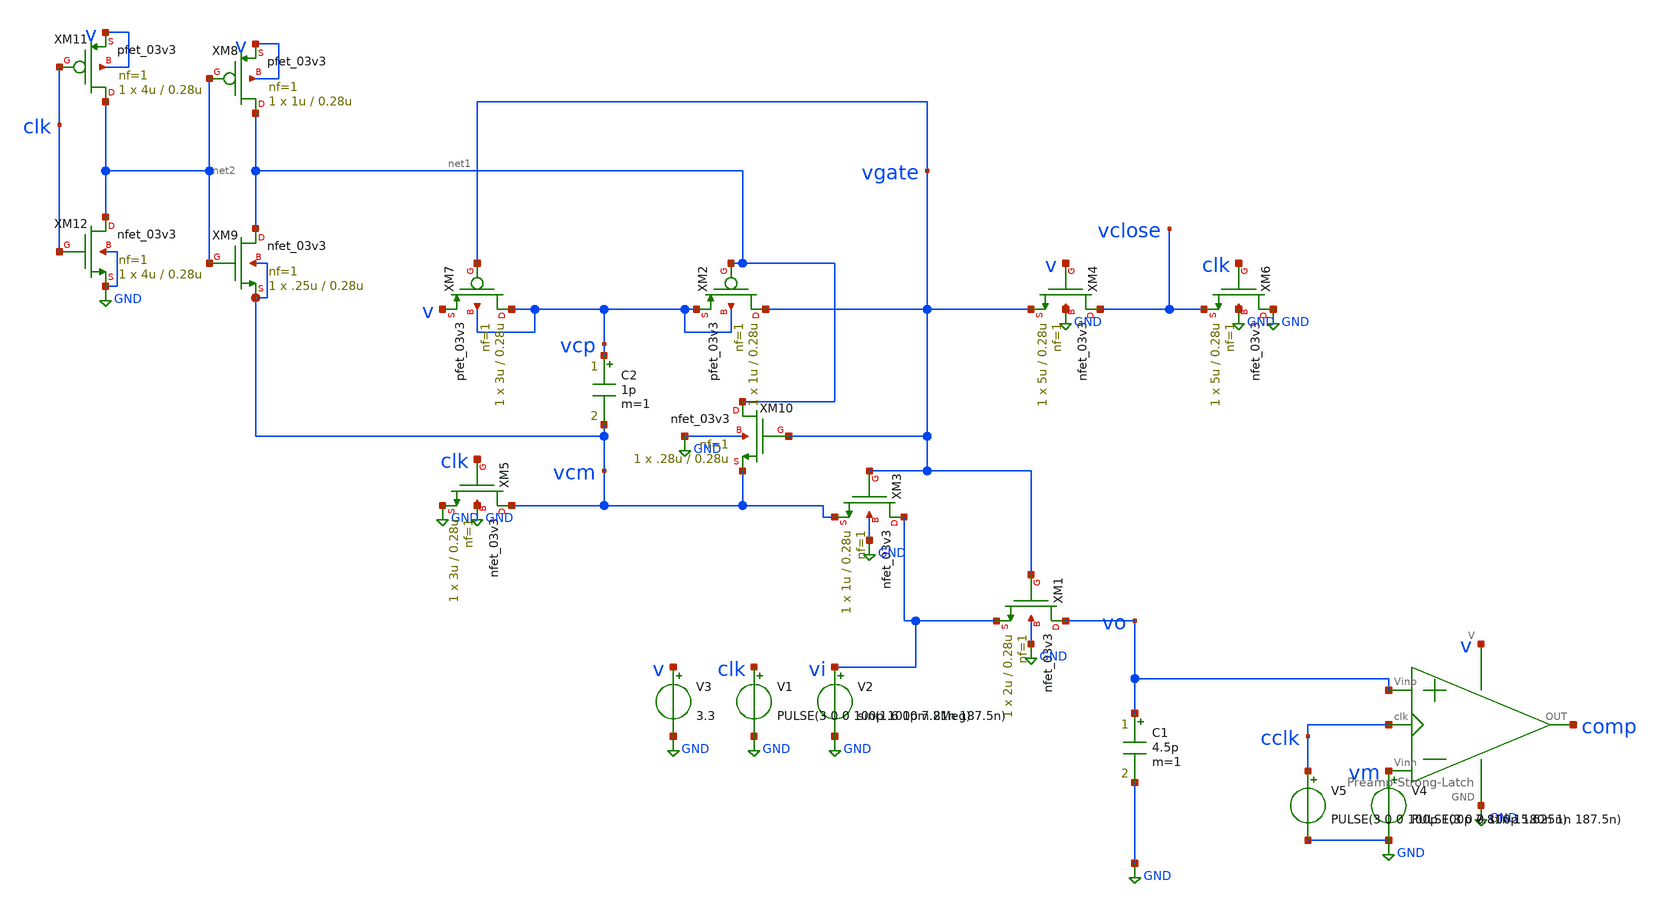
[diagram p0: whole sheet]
** sch_path: full_S&H/testbench/full__tb.sch
**.subckt full__tb
XM1 vo vgate vi GND nfet_03v3 L=0.28u W=2u nf=1 ad='int((nf+1)/2) * W/nf * 0.18u' as='int((nf+2)/2) * W/nf * 0.18u'
+ pd='2*int((nf+1)/2) * (W/nf + 0.18u)' ps='2*int((nf+2)/2) * (W/nf + 0.18u)' nrd='0.18u / W' nrs='0.18u / W'
+ sa=0 sb=0 sd=0 m=1
XM2 vgate net1 vcp vcp pfet_03v3 L=0.28u W=1u nf=1 ad='int((nf+1)/2) * W/nf * 0.18u' as='int((nf+2)/2) * W/nf * 0.18u'
+ pd='2*int((nf+1)/2) * (W/nf + 0.18u)' ps='2*int((nf+2)/2) * (W/nf + 0.18u)' nrd='0.18u / W' nrs='0.18u / W'
+ sa=0 sb=0 sd=0 m=1
XM3 vi vgate vcm GND nfet_03v3 L=0.28u W=1u nf=1 ad='int((nf+1)/2) * W/nf * 0.18u' as='int((nf+2)/2) * W/nf * 0.18u'
+ pd='2*int((nf+1)/2) * (W/nf + 0.18u)' ps='2*int((nf+2)/2) * (W/nf + 0.18u)' nrd='0.18u / W' nrs='0.18u / W'
+ sa=0 sb=0 sd=0 m=1
XM4 vclose v vgate GND nfet_03v3 L=0.28u W=5u nf=1 ad='int((nf+1)/2) * W/nf * 0.18u' as='int((nf+2)/2) * W/nf * 0.18u'
+ pd='2*int((nf+1)/2) * (W/nf + 0.18u)' ps='2*int((nf+2)/2) * (W/nf + 0.18u)' nrd='0.18u / W' nrs='0.18u / W'
+ sa=0 sb=0 sd=0 m=1
XM5 vcm clk GND GND nfet_03v3 L=0.28u W=3u nf=1 ad='int((nf+1)/2) * W/nf * 0.18u' as='int((nf+2)/2) * W/nf * 0.18u'
+ pd='2*int((nf+1)/2) * (W/nf + 0.18u)' ps='2*int((nf+2)/2) * (W/nf + 0.18u)' nrd='0.18u / W' nrs='0.18u / W'
+ sa=0 sb=0 sd=0 m=1
XM6 GND clk vclose GND nfet_03v3 L=0.28u W=5u nf=1 ad='int((nf+1)/2) * W/nf * 0.18u' as='int((nf+2)/2) * W/nf * 0.18u'
+ pd='2*int((nf+1)/2) * (W/nf + 0.18u)' ps='2*int((nf+2)/2) * (W/nf + 0.18u)' nrd='0.18u / W' nrs='0.18u / W'
+ sa=0 sb=0 sd=0 m=1
XM7 vcp vgate v vcp pfet_03v3 L=0.28u W=3u nf=1 ad='int((nf+1)/2) * W/nf * 0.18u' as='int((nf+2)/2) * W/nf * 0.18u'
+ pd='2*int((nf+1)/2) * (W/nf + 0.18u)' ps='2*int((nf+2)/2) * (W/nf + 0.18u)' nrd='0.18u / W' nrs='0.18u / W'
+ sa=0 sb=0 sd=0 m=1
XM8 net1 net2 v v pfet_03v3 L=0.28u W=1u nf=1 ad='int((nf+1)/2) * W/nf * 0.18u' as='int((nf+2)/2) * W/nf * 0.18u'
+ pd='2*int((nf+1)/2) * (W/nf + 0.18u)' ps='2*int((nf+2)/2) * (W/nf + 0.18u)' nrd='0.18u / W' nrs='0.18u / W'
+ sa=0 sb=0 sd=0 m=1
XM9 net1 net2 vcm vcm nfet_03v3 L=0.28u W=.25u nf=1 ad='int((nf+1)/2) * W/nf * 0.18u' as='int((nf+2)/2) * W/nf * 0.18u'
+ pd='2*int((nf+1)/2) * (W/nf + 0.18u)' ps='2*int((nf+2)/2) * (W/nf + 0.18u)' nrd='0.18u / W' nrs='0.18u / W'
+ sa=0 sb=0 sd=0 m=1
XM11 net2 clk v v pfet_03v3 L=0.28u W=4u nf=1 ad='int((nf+1)/2) * W/nf * 0.18u' as='int((nf+2)/2) * W/nf * 0.18u'
+ pd='2*int((nf+1)/2) * (W/nf + 0.18u)' ps='2*int((nf+2)/2) * (W/nf + 0.18u)' nrd='0.18u / W' nrs='0.18u / W'
+ sa=0 sb=0 sd=0 m=1
XM12 net2 clk GND GND nfet_03v3 L=0.28u W=4u nf=1 ad='int((nf+1)/2) * W/nf * 0.18u' as='int((nf+2)/2) * W/nf * 0.18u'
+ pd='2*int((nf+1)/2) * (W/nf + 0.18u)' ps='2*int((nf+2)/2) * (W/nf + 0.18u)' nrd='0.18u / W' nrs='0.18u / W'
+ sa=0 sb=0 sd=0 m=1
C1 vo GND 4.5p m=1
C2 vcp vcm 1p m=1
V2 vi GND sin(1.6 10m 2Meg)
V3 v GND 3.3
V1 clk GND PULSE(3 0 0 100p 100p 7.81n 187.5n)
XM10 net1 vgate vcm GND nfet_03v3 L=0.28u W=.28u nf=1 ad='int((nf+1)/2) * W/nf * 0.18u' as='int((nf+2)/2) * W/nf * 0.18u'
+ pd='2*int((nf+1)/2) * (W/nf + 0.18u)' ps='2*int((nf+2)/2) * (W/nf + 0.18u)' nrd='0.18u / W' nrs='0.18u / W'
+ sa=0 sb=0 sd=0 m=1
X1 v GND vo vm comp cclk Preamp-Strong-Latch
V4 vm GND PULSE(3 0 0 100p 180n 1n 187.5n)
V5 cclk GND PULSE(3 0 0 100p 100p 7.81n 15.625n)
**** begin user architecture code

.include /foss/pdks/gf180mcuC/libs.tech/ngspice/design.ngspice
.lib /foss/pdks/gf180mcuC/libs.tech/ngspice/sm141064.ngspice typical
.lib /foss/pdks/gf180mcuC/libs.tech/ngspice/sm141064.ngspice mimcap_statistical
.lib /foss/pdks/gf180mcuC/libs.tech/ngspice/sm141064.ngspice cap_mim



.control
save all
tran 50p 5u 3000n

plot {vi-vo}
plot vi vo
plot vgate vi
plot vi comp
plot {vo - vm} comp cclk
.endc

**** end user architecture code
**.ends
.GLOBAL GND
.end
